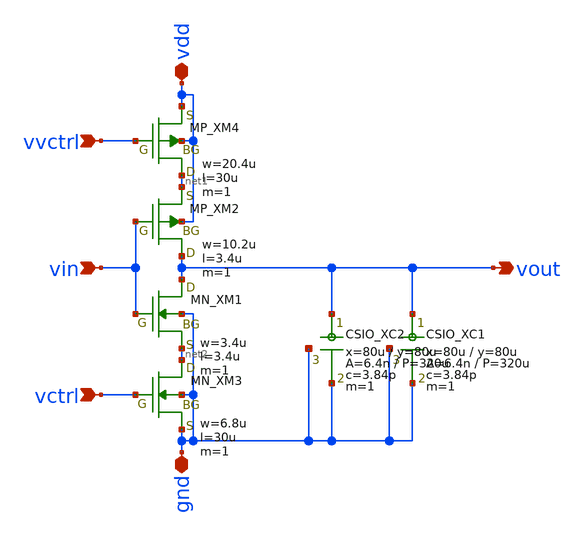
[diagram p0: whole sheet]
** sch_path: member_project/ringOSC/noritsuna/inverter.sch
**.subckt inverter vin vout vdd gnd vctrl vvctrl
*.ipin vin
*.opin vout
*.iopin vdd
*.iopin gnd
*.ipin vctrl
*.ipin vvctrl
XM1 vout vin net2 gnd NMOS w=3.4u l=3.4u as=0 ad=0 ps=0 pd=0 nrd=0 nrs=0 m=1
XM2 vout vin net1 vdd PMOS w=10.2u l=3.4u as=0 ad=0 ps=0 pd=0 nrd=0 nrs=0 m=1
XM3 net2 vctrl gnd gnd NMOS w=6.8u l=30u as=0 ad=0 ps=0 pd=0 nrd=0 nrs=0 m=1
XM4 net1 vvctrl vdd vdd PMOS w=20.4u l=30u as=0 ad=0 ps=0 pd=0 nrd=0 nrs=0 m=1
XXC1 vout gnd gnd F_CSIO c=3.84p x=80u y=80u m=1
XXC2 vout gnd gnd F_CSIO c=3.84p x=80u y=80u m=1
**.ends
.end
